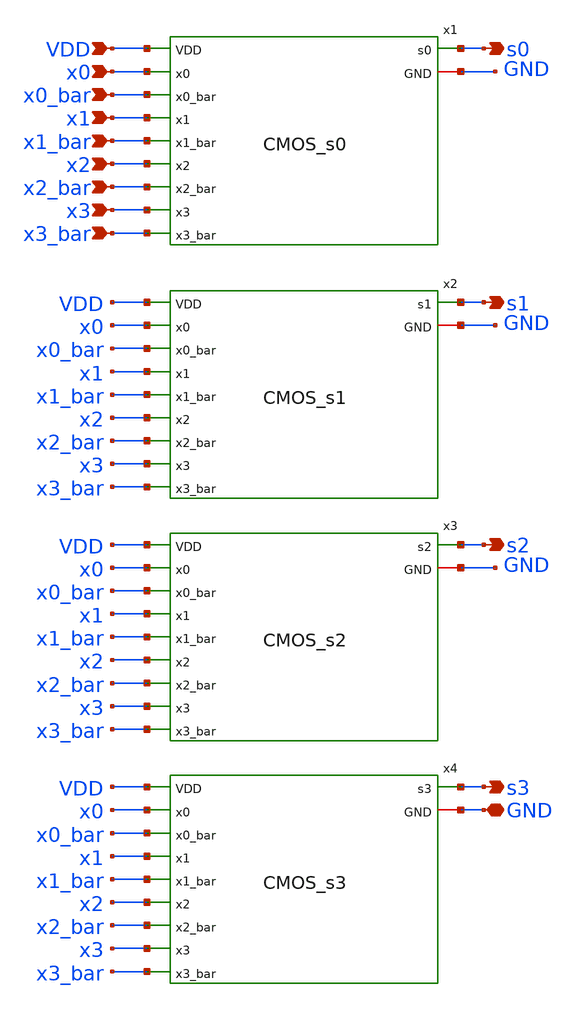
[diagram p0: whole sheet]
** sch_path: skywater_stuff/untitled-13.sch
**.subckt untitled-13 x0 x0_bar x1 x1_bar x2 x2_bar x3 x3_bar VDD GND s0 s1 s2 s3
*.ipin x0
*.ipin x0_bar
*.ipin x1
*.ipin x1_bar
*.ipin x2
*.ipin x2_bar
*.ipin x3
*.ipin x3_bar
*.ipin VDD
*.iopin GND
*.opin s0
*.opin s1
*.opin s2
*.opin s3
x1 GND x0 x0_bar x1 x1_bar x2 x2_bar x3 x3_bar VDD s0 CMOS_s0
x2 GND x0 x0_bar x1 x1_bar x2 x2_bar x3 VDD x3_bar s1 CMOS_s1
x3 GND x0 x0_bar x1 x1_bar x2 x2_bar x3 VDD x3_bar s2 CMOS_s2
x4 GND x0 x0_bar x1 x1_bar x2 x2_bar x3 VDD x3_bar s3 CMOS_s3
**.ends
.end
